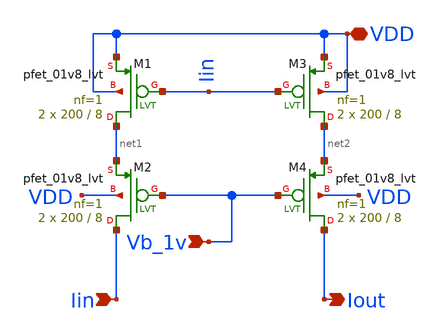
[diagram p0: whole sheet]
** sch_path: xschem/wideswing_cur_mir_pmos.sch
**.subckt wideswing_cur_mir_pmos Iout Iin Vb_1v VDD
*.opin Iout
*.ipin Iin
*.ipin Vb_1v
*.iopin VDD
XM1 net1 Iin VDD VDD sky130_fd_pr__pfet_01v8_lvt L=8 W=200 nf=1 ad='int((1 + 1)/2) * 200 / 1 * 0.29'
+ as='int((1 + 2)/2) * 200 / 1 * 0.29' pd='2*int((1 + 1)/2) * (200 / 1 + 0.29)' ps='2*int((1 + 2)/2) * (200 / 1 + 0.29)'
+ nrd='0.29 / 200 ' nrs='0.29 / 200 ' sa=0 sb=0 sd=0 mult=2 m=2
XM2 Iin Vb_1v net1 VDD sky130_fd_pr__pfet_01v8_lvt L=8 W=200 nf=1 ad='int((1 + 1)/2) * 200 / 1 * 0.29'
+ as='int((1 + 2)/2) * 200 / 1 * 0.29' pd='2*int((1 + 1)/2) * (200 / 1 + 0.29)' ps='2*int((1 + 2)/2) * (200 / 1 + 0.29)'
+ nrd='0.29 / 200 ' nrs='0.29 / 200 ' sa=0 sb=0 sd=0 mult=2 m=2
XM3 net2 Iin VDD VDD sky130_fd_pr__pfet_01v8_lvt L=8 W=200 nf=1 ad='int((1 + 1)/2) * 200 / 1 * 0.29'
+ as='int((1 + 2)/2) * 200 / 1 * 0.29' pd='2*int((1 + 1)/2) * (200 / 1 + 0.29)' ps='2*int((1 + 2)/2) * (200 / 1 + 0.29)'
+ nrd='0.29 / 200 ' nrs='0.29 / 200 ' sa=0 sb=0 sd=0 mult=2 m=2
XM4 Iout Vb_1v net2 VDD sky130_fd_pr__pfet_01v8_lvt L=8 W=200 nf=1 ad='int((1 + 1)/2) * 200 / 1 * 0.29'
+ as='int((1 + 2)/2) * 200 / 1 * 0.29' pd='2*int((1 + 1)/2) * (200 / 1 + 0.29)' ps='2*int((1 + 2)/2) * (200 / 1 + 0.29)'
+ nrd='0.29 / 200 ' nrs='0.29 / 200 ' sa=0 sb=0 sd=0 mult=2 m=2
**.ends
.end
